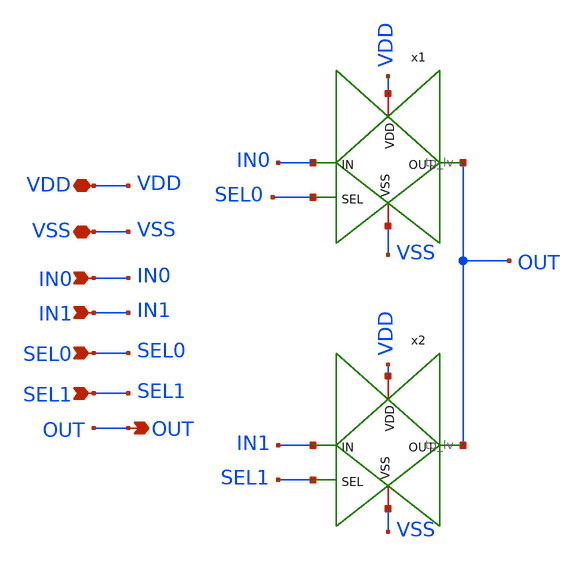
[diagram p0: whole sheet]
** sch_path: xschem/mux21.sch
**.subckt mux21 VDD VSS IN0 IN1 SEL0 SEL1 OUT
*.iopin VDD
*.iopin VSS
*.ipin IN0
*.ipin IN1
*.ipin SEL0
*.ipin SEL1
*.opin OUT
x1 VDD VSS SEL0 OUT IN0 tg_lv
x2 VDD VSS SEL1 OUT IN1 tg_lv
**.ends
.end
